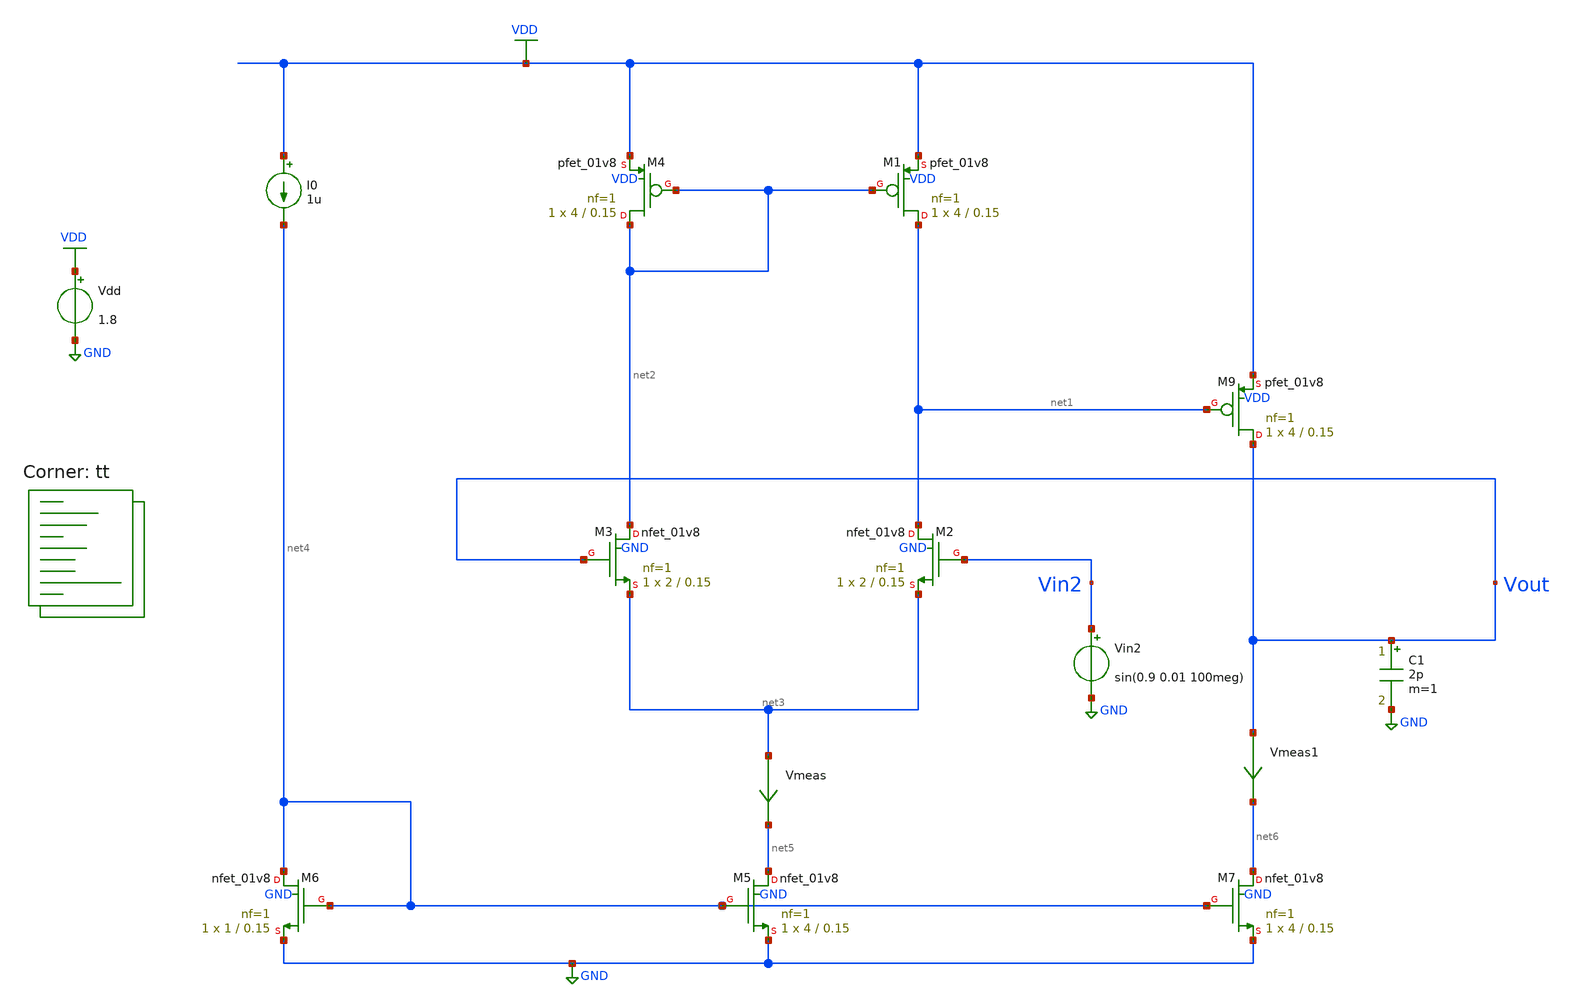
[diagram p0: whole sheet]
** sch_path: projects/pll/trials/opamp2.sch
**.subckt opamp2
XM1 net1 net2 VDD VDD sky130_fd_pr__pfet_01v8 L=0.15 W=4 nf=1 ad='int((nf+1)/2) * W/nf * 0.29' as='int((nf+2)/2) * W/nf * 0.29'
+ pd='2*int((nf+1)/2) * (W/nf + 0.29)' ps='2*int((nf+2)/2) * (W/nf + 0.29)' nrd='0.29 / W' nrs='0.29 / W'
+ sa=0 sb=0 sd=0 mult=1 m=1
XM2 net1 Vin2 net3 GND sky130_fd_pr__nfet_01v8 L=0.15 W=2 nf=1 ad='int((nf+1)/2) * W/nf * 0.29' as='int((nf+2)/2) * W/nf * 0.29'
+ pd='2*int((nf+1)/2) * (W/nf + 0.29)' ps='2*int((nf+2)/2) * (W/nf + 0.29)' nrd='0.29 / W' nrs='0.29 / W'
+ sa=0 sb=0 sd=0 mult=1 m=1
XM3 net2 Vout net3 GND sky130_fd_pr__nfet_01v8 L=0.15 W=2 nf=1 ad='int((nf+1)/2) * W/nf * 0.29' as='int((nf+2)/2) * W/nf * 0.29'
+ pd='2*int((nf+1)/2) * (W/nf + 0.29)' ps='2*int((nf+2)/2) * (W/nf + 0.29)' nrd='0.29 / W' nrs='0.29 / W'
+ sa=0 sb=0 sd=0 mult=1 m=1
XM4 net2 net2 VDD VDD sky130_fd_pr__pfet_01v8 L=0.15 W=4 nf=1 ad='int((nf+1)/2) * W/nf * 0.29' as='int((nf+2)/2) * W/nf * 0.29'
+ pd='2*int((nf+1)/2) * (W/nf + 0.29)' ps='2*int((nf+2)/2) * (W/nf + 0.29)' nrd='0.29 / W' nrs='0.29 / W'
+ sa=0 sb=0 sd=0 mult=1 m=1
I0 VDD net4 1u
XM7 net6 net4 GND GND sky130_fd_pr__nfet_01v8 L=0.15 W=4 nf=1 ad='int((nf+1)/2) * W/nf * 0.29' as='int((nf+2)/2) * W/nf * 0.29'
+ pd='2*int((nf+1)/2) * (W/nf + 0.29)' ps='2*int((nf+2)/2) * (W/nf + 0.29)' nrd='0.29 / W' nrs='0.29 / W'
+ sa=0 sb=0 sd=0 mult=1 m=1
XM9 Vout net1 VDD VDD sky130_fd_pr__pfet_01v8 L=0.15 W=4 nf=1 ad='int((nf+1)/2) * W/nf * 0.29' as='int((nf+2)/2) * W/nf * 0.29'
+ pd='2*int((nf+1)/2) * (W/nf + 0.29)' ps='2*int((nf+2)/2) * (W/nf + 0.29)' nrd='0.29 / W' nrs='0.29 / W'
+ sa=0 sb=0 sd=0 mult=1 m=1
Vdd VDD GND 1.8
XM5 net5 net4 GND GND sky130_fd_pr__nfet_01v8 L=0.15 W=4 nf=1 ad='int((nf+1)/2) * W/nf * 0.29' as='int((nf+2)/2) * W/nf * 0.29'
+ pd='2*int((nf+1)/2) * (W/nf + 0.29)' ps='2*int((nf+2)/2) * (W/nf + 0.29)' nrd='0.29 / W' nrs='0.29 / W'
+ sa=0 sb=0 sd=0 mult=1 m=1
XM6 net4 net4 GND GND sky130_fd_pr__nfet_01v8 L=0.15 W=1 nf=1 ad='int((nf+1)/2) * W/nf * 0.29' as='int((nf+2)/2) * W/nf * 0.29'
+ pd='2*int((nf+1)/2) * (W/nf + 0.29)' ps='2*int((nf+2)/2) * (W/nf + 0.29)' nrd='0.29 / W' nrs='0.29 / W'
+ sa=0 sb=0 sd=0 mult=1 m=1
Vmeas net3 net5 0
.save i(vmeas)
Vmeas1 Vout net6 0
.save i(vmeas1)
Vin2 Vin2 GND sin(0.9 0.01 100meg)
C1 Vout GND 2p m=1
**** begin user architecture code



.option wnflag=1

.control

  save all
  tran 10p 200n
  * dc Vin2 0 1.8 0.001
  * ac dec 20 1 1e12
  * let Tmag = db(v(Vout))
  * let Tphase = 180*cph(v(Vout))/pi
  write opamp2.raw
  set appendwrite

.endc



.lib $::SKYWATER_MODELS/sky130.lib.spice tt
**** end user architecture code
**.ends
.GLOBAL GND
.GLOBAL VDD
.end
